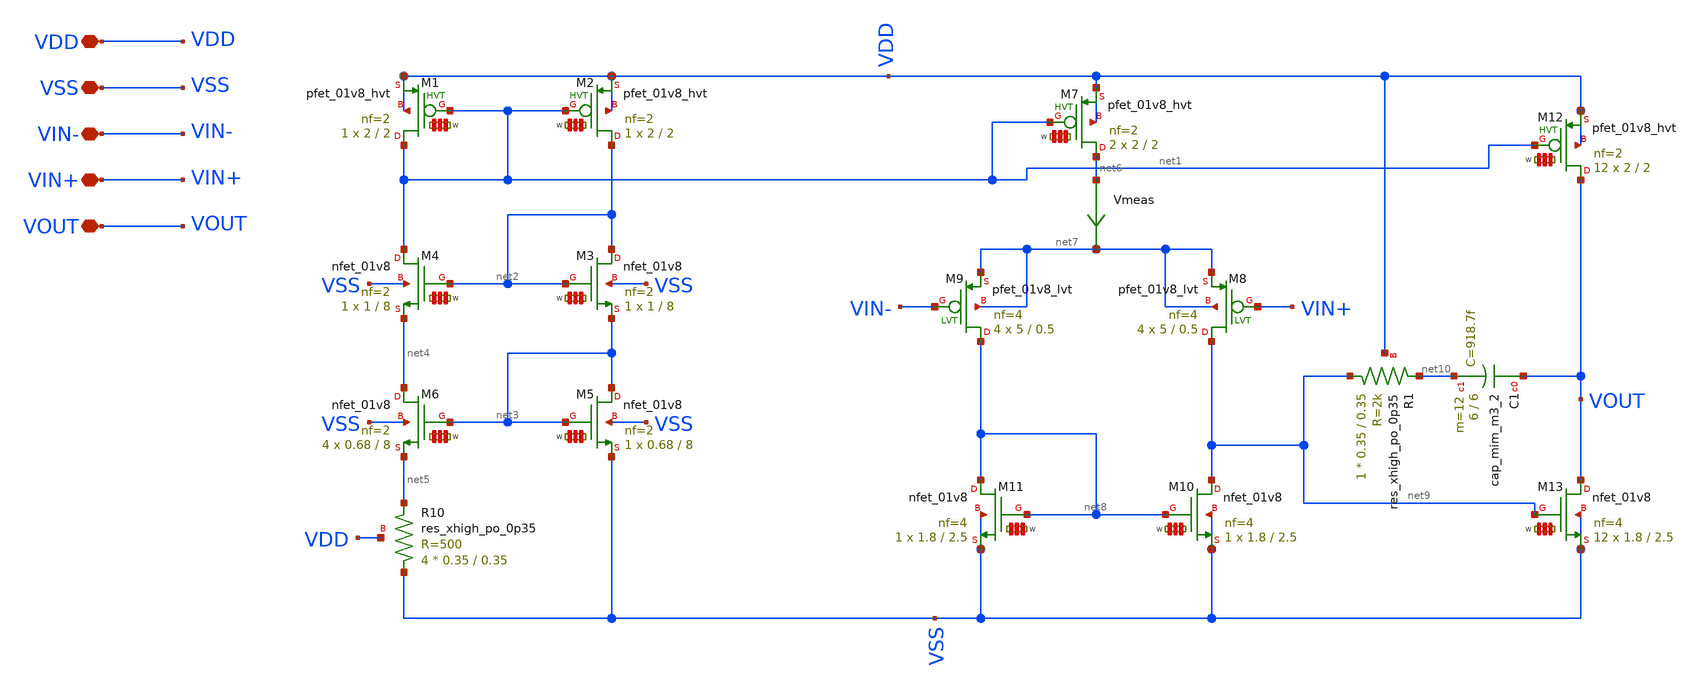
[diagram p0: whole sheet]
** sch_path: my_ip/sky130A/2_stage_op_amp_sky130/op_amp.sch
**.subckt op_amp VDD VSS VIN- VIN+ VOUT
*.iopin VDD
*.iopin VSS
*.iopin VIN-
*.iopin VIN+
*.iopin VOUT
XM5 net3 net3 VSS VSS sky130_fd_pr__nfet_01v8 L=8 W='0.68 * 2 ' nf=2 ad='int((2 + 1)/2) * 0.68 / 2 * 0.29'
+ as='int((2 + 2)/2) * 0.68 / 2 * 0.29' pd='2*int((2 + 1)/2) * (0.68 / 2 + 0.29)' ps='2*int((2 + 2)/2) * (0.68 / 2 + 0.29)'
+ nrd='0.29 / 0.68 ' nrs='0.29 / 0.68 ' sa=0 sb=0 sd=0 mult=1 m=1
XM6 net4 net3 net5 VSS sky130_fd_pr__nfet_01v8 L=8 W='0.68 * 2 ' nf=2 ad='int((2 + 1)/2) * 0.68 / 2 * 0.29'
+ as='int((2 + 2)/2) * 0.68 / 2 * 0.29' pd='2*int((2 + 1)/2) * (0.68 / 2 + 0.29)' ps='2*int((2 + 2)/2) * (0.68 / 2 + 0.29)'
+ nrd='0.29 / 0.68 ' nrs='0.29 / 0.68 ' sa=0 sb=0 sd=0 mult=4 m=4
Vmeas net6 net7 0
.save i(vmeas)
XM7 net6 net1 VDD VDD sky130_fd_pr__pfet_01v8_hvt L=2 W='2 * 2 ' nf=2 ad='int((2 + 1)/2) * 2 / 2 * 0.29'
+ as='int((2 + 2)/2) * 2 / 2 * 0.29' pd='2*int((2 + 1)/2) * (2 / 2 + 0.29)' ps='2*int((2 + 2)/2) * (2 / 2 + 0.29)'
+ nrd='0.29 / 2 ' nrs='0.29 / 2 ' sa=0 sb=0 sd=0 mult=2 m=2
XM2 net2 net1 VDD VDD sky130_fd_pr__pfet_01v8_hvt L=2 W='2 * 2 ' nf=2 ad='int((2 + 1)/2) * 2 / 2 * 0.29'
+ as='int((2 + 2)/2) * 2 / 2 * 0.29' pd='2*int((2 + 1)/2) * (2 / 2 + 0.29)' ps='2*int((2 + 2)/2) * (2 / 2 + 0.29)'
+ nrd='0.29 / 2 ' nrs='0.29 / 2 ' sa=0 sb=0 sd=0 mult=1 m=1
XM1 net1 net1 VDD VDD sky130_fd_pr__pfet_01v8_hvt L=2 W='2 * 2 ' nf=2 ad='int((2 + 1)/2) * 2 / 2 * 0.29'
+ as='int((2 + 2)/2) * 2 / 2 * 0.29' pd='2*int((2 + 1)/2) * (2 / 2 + 0.29)' ps='2*int((2 + 2)/2) * (2 / 2 + 0.29)'
+ nrd='0.29 / 2 ' nrs='0.29 / 2 ' sa=0 sb=0 sd=0 mult=1 m=1
XR10 VSS net5 VDD sky130_fd_pr__res_xhigh_po_0p35 L=0.35 mult=4 m=4
XM4 net1 net2 net4 VSS sky130_fd_pr__nfet_01v8 L=8 W='1 * 2 ' nf=2 ad='int((2 + 1)/2) * 1 / 2 * 0.29'
+ as='int((2 + 2)/2) * 1 / 2 * 0.29' pd='2*int((2 + 1)/2) * (1 / 2 + 0.29)' ps='2*int((2 + 2)/2) * (1 / 2 + 0.29)'
+ nrd='0.29 / 1 ' nrs='0.29 / 1 ' sa=0 sb=0 sd=0 mult=1 m=1
XM3 net2 net2 net3 VSS sky130_fd_pr__nfet_01v8 L=8 W='1 * 2 ' nf=2 ad='int((2 + 1)/2) * 1 / 2 * 0.29'
+ as='int((2 + 2)/2) * 1 / 2 * 0.29' pd='2*int((2 + 1)/2) * (1 / 2 + 0.29)' ps='2*int((2 + 2)/2) * (1 / 2 + 0.29)'
+ nrd='0.29 / 1 ' nrs='0.29 / 1 ' sa=0 sb=0 sd=0 mult=1 m=1
XM8 net9 VIN+ net7 net7 sky130_fd_pr__pfet_01v8_lvt L=0.5 W=5 nf=4 ad='int((4 + 1)/2) * 5 / 4 * 0.29'
+ as='int((4 + 2)/2) * 5 / 4 * 0.29' pd='2*int((4 + 1)/2) * (5 / 4 + 0.29)' ps='2*int((4 + 2)/2) * (5 / 4 + 0.29)'
+ nrd='0.29 / 5 ' nrs='0.29 / 5 ' sa=0 sb=0 sd=0 mult=4 m=4
XM9 net8 VIN- net7 net7 sky130_fd_pr__pfet_01v8_lvt L=0.5 W=5 nf=4 ad='int((4 + 1)/2) * 5 / 4 * 0.29'
+ as='int((4 + 2)/2) * 5 / 4 * 0.29' pd='2*int((4 + 1)/2) * (5 / 4 + 0.29)' ps='2*int((4 + 2)/2) * (5 / 4 + 0.29)'
+ nrd='0.29 / 5 ' nrs='0.29 / 5 ' sa=0 sb=0 sd=0 mult=4 m=4
XM10 net9 net8 VSS VSS sky130_fd_pr__nfet_01v8 L=2.5 W='1.8 * 4 ' nf=4 ad='int((4 + 1)/2) * 1.8 / 4 * 0.29'
+ as='int((4 + 2)/2) * 1.8 / 4 * 0.29' pd='2*int((4 + 1)/2) * (1.8 / 4 + 0.29)' ps='2*int((4 + 2)/2) * (1.8 / 4 + 0.29)'
+ nrd='0.29 / 1.8 ' nrs='0.29 / 1.8 ' sa=0 sb=0 sd=0 mult=1 m=1
XM11 net8 net8 VSS VSS sky130_fd_pr__nfet_01v8 L=2.5 W='1.8 * 4 ' nf=4 ad='int((4 + 1)/2) * 1.8 / 4 * 0.29'
+ as='int((4 + 2)/2) * 1.8 / 4 * 0.29' pd='2*int((4 + 1)/2) * (1.8 / 4 + 0.29)' ps='2*int((4 + 2)/2) * (1.8 / 4 + 0.29)'
+ nrd='0.29 / 1.8 ' nrs='0.29 / 1.8 ' sa=0 sb=0 sd=0 mult=1 m=1
XM12 VOUT net1 VDD VDD sky130_fd_pr__pfet_01v8_hvt L=2 W='2 * 2 ' nf=2 ad='int((2 + 1)/2) * 2 / 2 * 0.29'
+ as='int((2 + 2)/2) * 2 / 2 * 0.29' pd='2*int((2 + 1)/2) * (2 / 2 + 0.29)' ps='2*int((2 + 2)/2) * (2 / 2 + 0.29)'
+ nrd='0.29 / 2 ' nrs='0.29 / 2 ' sa=0 sb=0 sd=0 mult=12 m=12
XM13 VOUT net9 VSS VSS sky130_fd_pr__nfet_01v8 L=2.5 W='1.8 * 4 ' nf=4 ad='int((4 + 1)/2) * 1.8 / 4 * 0.29'
+ as='int((4 + 2)/2) * 1.8 / 4 * 0.29' pd='2*int((4 + 1)/2) * (1.8 / 4 + 0.29)' ps='2*int((4 + 2)/2) * (1.8 / 4 + 0.29)'
+ nrd='0.29 / 1.8 ' nrs='0.29 / 1.8 ' sa=0 sb=0 sd=0 mult=12 m=12
XC1 VOUT net10 sky130_fd_pr__cap_mim_m3_2 W=6 L=6 MF=12 m=12
XR1 net9 net10 VDD sky130_fd_pr__res_xhigh_po_0p35 L=0.35 mult=1 m=1
**.ends
.end
